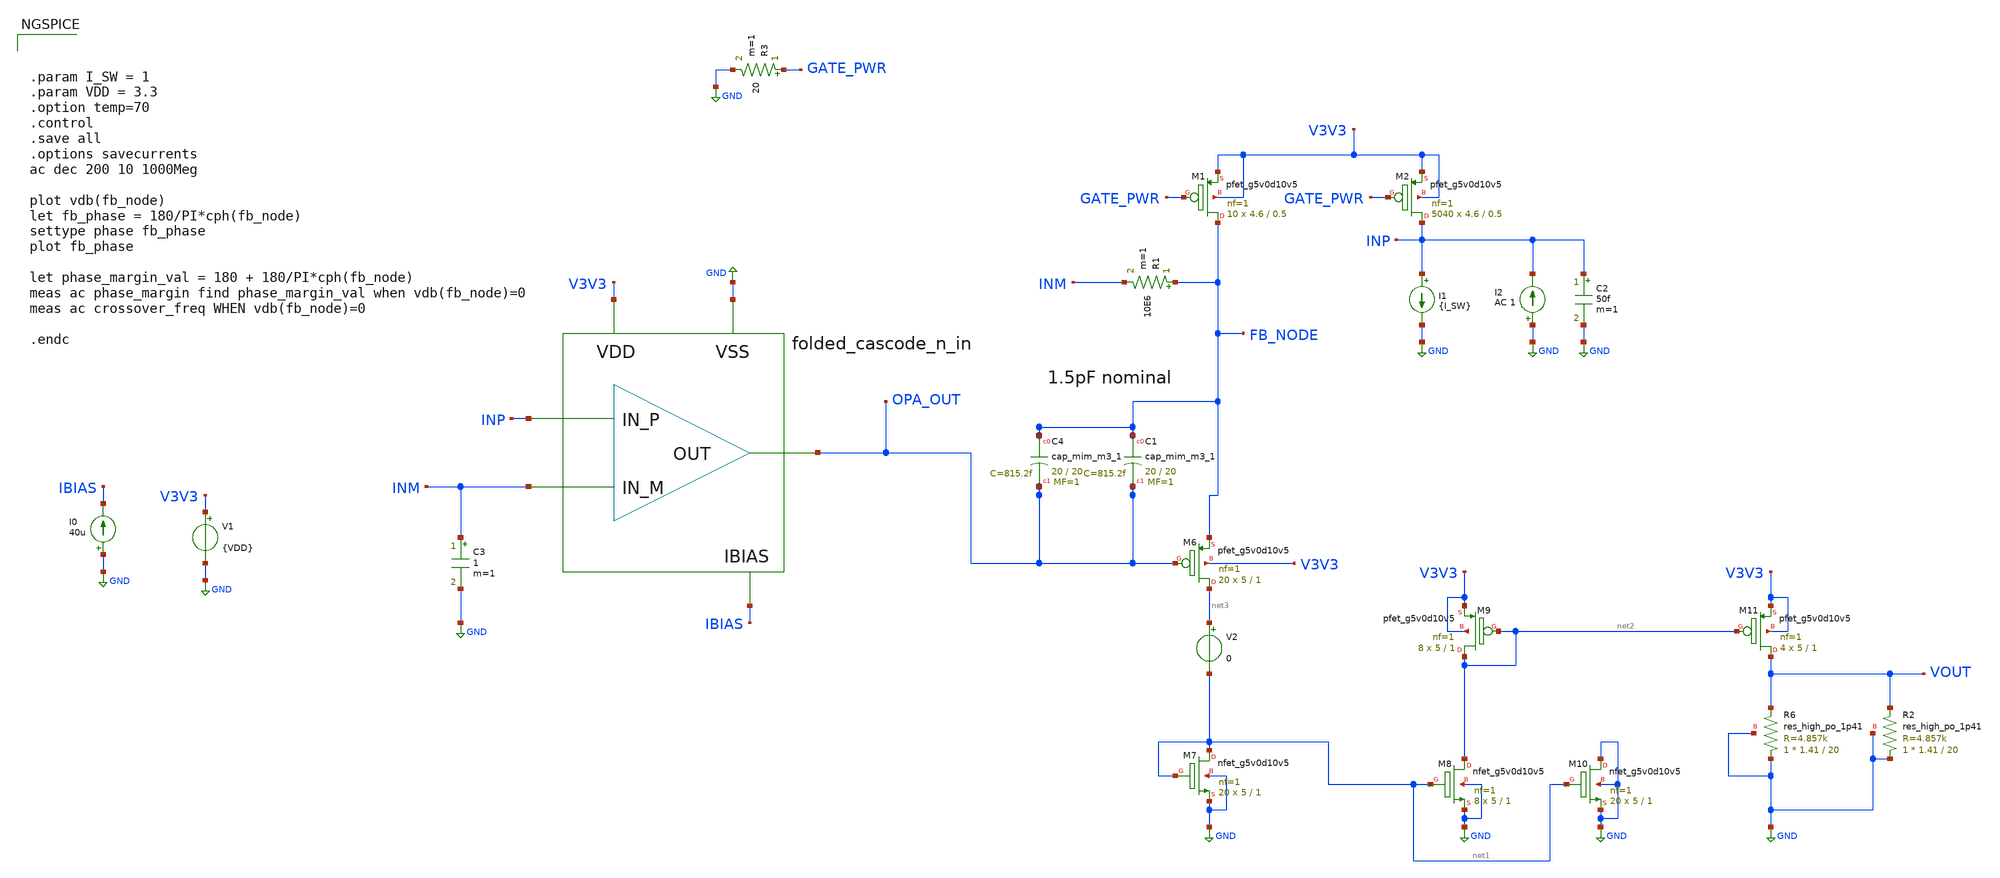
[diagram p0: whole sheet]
** sch_path: design/current-sense/current_sense_ac_phase_margin.sch
**.subckt current_sense_ac_phase_margin
V1 V3V3 GND {VDD}
I0 GND IBIAS 40u
x1 INP INM OPA_OUT V3V3 GND IBIAS folded_cascode_n_in
XM1 FB_NODE GATE_PWR V3V3 V3V3 sky130_fd_pr__pfet_g5v0d10v5 L=0.5 W=4.6 nf=1 ad='int((nf+1)/2) * W/nf * 0.29'
+ as='int((nf+2)/2) * W/nf * 0.29' pd='2*int((nf+1)/2) * (W/nf + 0.29)' ps='2*int((nf+2)/2) * (W/nf + 0.29)'
+ nrd='0.29 / W' nrs='0.29 / W' sa=0 sb=0 sd=0 mult=10 m=10
XM2 INP GATE_PWR V3V3 V3V3 sky130_fd_pr__pfet_g5v0d10v5 L=0.5 W=4.6 nf=1 ad='int((nf+1)/2) * W/nf * 0.29'
+ as='int((nf+2)/2) * W/nf * 0.29' pd='2*int((nf+1)/2) * (W/nf + 0.29)' ps='2*int((nf+2)/2) * (W/nf + 0.29)'
+ nrd='0.29 / W' nrs='0.29 / W' sa=0 sb=0 sd=0 mult=5040 m=5040
R3 GATE_PWR GND 20 m=1
I1 INP GND {I_SW}
I2 GND INP AC 1
C2 INP GND 50f m=1
XM6 net3 OPA_OUT FB_NODE V3V3 sky130_fd_pr__pfet_g5v0d10v5 L=1 W=5 nf=1 ad='int((nf+1)/2) * W/nf * 0.29'
+ as='int((nf+2)/2) * W/nf * 0.29' pd='2*int((nf+1)/2) * (W/nf + 0.29)' ps='2*int((nf+2)/2) * (W/nf + 0.29)'
+ nrd='0.29 / W' nrs='0.29 / W' sa=0 sb=0 sd=0 mult=20 m=20
XM7 net1 net1 GND GND sky130_fd_pr__nfet_g5v0d10v5 L=1 W=5 nf=1 ad='int((nf+1)/2) * W/nf * 0.29' as='int((nf+2)/2) * W/nf * 0.29'
+ pd='2*int((nf+1)/2) * (W/nf + 0.29)' ps='2*int((nf+2)/2) * (W/nf + 0.29)' nrd='0.29 / W' nrs='0.29 / W'
+ sa=0 sb=0 sd=0 mult=20 m=20
XM8 net2 net1 GND GND sky130_fd_pr__nfet_g5v0d10v5 L=1 W=5 nf=1 ad='int((nf+1)/2) * W/nf * 0.29' as='int((nf+2)/2) * W/nf * 0.29'
+ pd='2*int((nf+1)/2) * (W/nf + 0.29)' ps='2*int((nf+2)/2) * (W/nf + 0.29)' nrd='0.29 / W' nrs='0.29 / W'
+ sa=0 sb=0 sd=0 mult=8 m=8
XM9 net2 net2 V3V3 V3V3 sky130_fd_pr__pfet_g5v0d10v5 L=1 W=5 nf=1 ad='int((nf+1)/2) * W/nf * 0.29' as='int((nf+2)/2) * W/nf * 0.29'
+ pd='2*int((nf+1)/2) * (W/nf + 0.29)' ps='2*int((nf+2)/2) * (W/nf + 0.29)' nrd='0.29 / W' nrs='0.29 / W'
+ sa=0 sb=0 sd=0 mult=8 m=8
XM10 GND net1 GND GND sky130_fd_pr__nfet_g5v0d10v5 L=1 W=5 nf=1 ad='int((nf+1)/2) * W/nf * 0.29' as='int((nf+2)/2) * W/nf * 0.29'
+ pd='2*int((nf+1)/2) * (W/nf + 0.29)' ps='2*int((nf+2)/2) * (W/nf + 0.29)' nrd='0.29 / W' nrs='0.29 / W'
+ sa=0 sb=0 sd=0 mult=20 m=20
XM11 VOUT net2 V3V3 V3V3 sky130_fd_pr__pfet_g5v0d10v5 L=1 W=5 nf=1 ad='int((nf+1)/2) * W/nf * 0.29' as='int((nf+2)/2) * W/nf * 0.29'
+ pd='2*int((nf+1)/2) * (W/nf + 0.29)' ps='2*int((nf+2)/2) * (W/nf + 0.29)' nrd='0.29 / W' nrs='0.29 / W'
+ sa=0 sb=0 sd=0 mult=4 m=4
XR6 GND VOUT GND sky130_fd_pr__res_high_po_1p41 L=20 mult=1 m=1
XR2 GND VOUT GND sky130_fd_pr__res_high_po_1p41 L=20 mult=1 m=1
V2 net3 net1 0
XC4 FB_NODE OPA_OUT sky130_fd_pr__cap_mim_m3_1 W=20 L=20 MF=1 m=1
XC1 FB_NODE OPA_OUT sky130_fd_pr__cap_mim_m3_1 W=20 L=20 MF=1 m=1
R1 FB_NODE INM 10E6 m=1
C3 INM GND 1 m=1
**** begin user architecture code



.param I_SW = 1
.param VDD = 3.3
.option temp=70
.control
.save all
.options savecurrents
ac dec 200 10 1000Meg

plot vdb(fb_node)
let fb_phase = 180/PI*cph(fb_node)
settype phase fb_phase
plot fb_phase

let phase_margin_val = 180 + 180/PI*cph(fb_node)
meas ac phase_margin find phase_margin_val when vdb(fb_node)=0
meas ac crossover_freq WHEN vdb(fb_node)=0

.endc



.lib $::SKYWATER_MODELS/models/sky130.lib.spice tt
.option wnflag=1

**** end user architecture code
**.ends

* expanding   symbol:  design/folded-cascode-n-in/folded_cascode_n_in.sym # of pins=6
** sym_path: design/folded-cascode-n-in/folded_cascode_n_in.sym
** sch_path: design/folded-cascode-n-in/folded_cascode_n_in.sch
.subckt folded_cascode_n_in IN_P IN_M OUT VDD VSS VBN
*.ipin IN_P
*.ipin IN_M
*.ipin OUT
*.ipin VDD
*.ipin VSS
*.ipin VBN
XM1 net1 VBN VSS VSS sky130_fd_pr__nfet_g5v0d10v5 L=1 W=5 nf=1 ad='int((nf+1)/2) * W/nf * 0.29' as='int((nf+2)/2) * W/nf * 0.29'
+ pd='2*int((nf+1)/2) * (W/nf + 0.29)' ps='2*int((nf+2)/2) * (W/nf + 0.29)' nrd='0.29 / W' nrs='0.29 / W'
+ sa=0 sb=0 sd=0 mult=12 m=12
XM3 VS1_P IN_M net1 VSS sky130_fd_pr__nfet_g5v0d10v5 L=1 W=5 nf=1 ad='int((nf+1)/2) * W/nf * 0.29' as='int((nf+2)/2) * W/nf * 0.29'
+ pd='2*int((nf+1)/2) * (W/nf + 0.29)' ps='2*int((nf+2)/2) * (W/nf + 0.29)' nrd='0.29 / W' nrs='0.29 / W'
+ sa=0 sb=0 sd=0 mult=24 m=24
XM4 VS1_M IN_P net1 VSS sky130_fd_pr__nfet_g5v0d10v5 L=1 W=5 nf=1 ad='int((nf+1)/2) * W/nf * 0.29' as='int((nf+2)/2) * W/nf * 0.29'
+ pd='2*int((nf+1)/2) * (W/nf + 0.29)' ps='2*int((nf+2)/2) * (W/nf + 0.29)' nrd='0.29 / W' nrs='0.29 / W'
+ sa=0 sb=0 sd=0 mult=24 m=24
XM9 net2 VCN net4 VSS sky130_fd_pr__nfet_g5v0d10v5 L=1 W=5 nf=1 ad='int((nf+1)/2) * W/nf * 0.29' as='int((nf+2)/2) * W/nf * 0.29'
+ pd='2*int((nf+1)/2) * (W/nf + 0.29)' ps='2*int((nf+2)/2) * (W/nf + 0.29)' nrd='0.29 / W' nrs='0.29 / W'
+ sa=0 sb=0 sd=0 mult=3 m=3
XM10 net3 net2 VSS VSS sky130_fd_pr__nfet_g5v0d10v5 L=1 W=5 nf=1 ad='int((nf+1)/2) * W/nf * 0.29' as='int((nf+2)/2) * W/nf * 0.29'
+ pd='2*int((nf+1)/2) * (W/nf + 0.29)' ps='2*int((nf+2)/2) * (W/nf + 0.29)' nrd='0.29 / W' nrs='0.29 / W'
+ sa=0 sb=0 sd=0 mult=3 m=3
XM11 net4 net2 VSS VSS sky130_fd_pr__nfet_g5v0d10v5 L=1 W=5 nf=1 ad='int((nf+1)/2) * W/nf * 0.29' as='int((nf+2)/2) * W/nf * 0.29'
+ pd='2*int((nf+1)/2) * (W/nf + 0.29)' ps='2*int((nf+2)/2) * (W/nf + 0.29)' nrd='0.29 / W' nrs='0.29 / W'
+ sa=0 sb=0 sd=0 mult=3 m=3
XM12 OUT VCN net3 VSS sky130_fd_pr__nfet_g5v0d10v5 L=1 W=5 nf=1 ad='int((nf+1)/2) * W/nf * 0.29' as='int((nf+2)/2) * W/nf * 0.29'
+ pd='2*int((nf+1)/2) * (W/nf + 0.29)' ps='2*int((nf+2)/2) * (W/nf + 0.29)' nrd='0.29 / W' nrs='0.29 / W'
+ sa=0 sb=0 sd=0 mult=3 m=3
XM5 VS1_P VBP_INT VDD VDD sky130_fd_pr__pfet_g5v0d10v5 L=1 W=5 nf=1 ad='int((nf+1)/2) * W/nf * 0.29'
+ as='int((nf+2)/2) * W/nf * 0.29' pd='2*int((nf+1)/2) * (W/nf + 0.29)' ps='2*int((nf+2)/2) * (W/nf + 0.29)'
+ nrd='0.29 / W' nrs='0.29 / W' sa=0 sb=0 sd=0 mult=9 m=9
XM13 VS1_M VBP_INT VDD VDD sky130_fd_pr__pfet_g5v0d10v5 L=1 W=5 nf=1 ad='int((nf+1)/2) * W/nf * 0.29'
+ as='int((nf+2)/2) * W/nf * 0.29' pd='2*int((nf+1)/2) * (W/nf + 0.29)' ps='2*int((nf+2)/2) * (W/nf + 0.29)'
+ nrd='0.29 / W' nrs='0.29 / W' sa=0 sb=0 sd=0 mult=9 m=9
XM17 VBP_INT VBN VSS VSS sky130_fd_pr__nfet_g5v0d10v5 L=1 W=5 nf=1 ad='int((nf+1)/2) * W/nf * 0.29' as='int((nf+2)/2) * W/nf * 0.29'
+ pd='2*int((nf+1)/2) * (W/nf + 0.29)' ps='2*int((nf+2)/2) * (W/nf + 0.29)' nrd='0.29 / W' nrs='0.29 / W'
+ sa=0 sb=0 sd=0 mult=1 m=1
XM18 VBP_INT VBP_INT VDD VDD sky130_fd_pr__pfet_g5v0d10v5 L=1 W=5 nf=1 ad='int((nf+1)/2) * W/nf * 0.29'
+ as='int((nf+2)/2) * W/nf * 0.29' pd='2*int((nf+1)/2) * (W/nf + 0.29)' ps='2*int((nf+2)/2) * (W/nf + 0.29)'
+ nrd='0.29 / W' nrs='0.29 / W' sa=0 sb=0 sd=0 mult=1 m=1
XM14 net2 VCP VS1_M VDD sky130_fd_pr__pfet_g5v0d10v5 L=1 W=5 nf=1 ad='int((nf+1)/2) * W/nf * 0.29' as='int((nf+2)/2) * W/nf * 0.29'
+ pd='2*int((nf+1)/2) * (W/nf + 0.29)' ps='2*int((nf+2)/2) * (W/nf + 0.29)' nrd='0.29 / W' nrs='0.29 / W'
+ sa=0 sb=0 sd=0 mult=3 m=3
XM19 OUT VCP VS1_P VDD sky130_fd_pr__pfet_g5v0d10v5 L=1 W=5 nf=1 ad='int((nf+1)/2) * W/nf * 0.29' as='int((nf+2)/2) * W/nf * 0.29'
+ pd='2*int((nf+1)/2) * (W/nf + 0.29)' ps='2*int((nf+2)/2) * (W/nf + 0.29)' nrd='0.29 / W' nrs='0.29 / W'
+ sa=0 sb=0 sd=0 mult=3 m=3
XM2 VBP_INT VBP_INT VS1_P VSS sky130_fd_pr__nfet_g5v0d10v5 L=1 W=5 nf=1 ad='int((nf+1)/2) * W/nf * 0.29'
+ as='int((nf+2)/2) * W/nf * 0.29' pd='2*int((nf+1)/2) * (W/nf + 0.29)' ps='2*int((nf+2)/2) * (W/nf + 0.29)'
+ nrd='0.29 / W' nrs='0.29 / W' sa=0 sb=0 sd=0 mult=1 m=1
XM6 VBP_INT VBP_INT VS1_M VSS sky130_fd_pr__nfet_g5v0d10v5 L=1 W=5 nf=1 ad='int((nf+1)/2) * W/nf * 0.29'
+ as='int((nf+2)/2) * W/nf * 0.29' pd='2*int((nf+1)/2) * (W/nf + 0.29)' ps='2*int((nf+2)/2) * (W/nf + 0.29)'
+ nrd='0.29 / W' nrs='0.29 / W' sa=0 sb=0 sd=0 mult=1 m=1
XM7 VBP VBP VDD VDD sky130_fd_pr__pfet_g5v0d10v5 L=1 W=5 nf=1 ad='int((nf+1)/2) * W/nf * 0.29' as='int((nf+2)/2) * W/nf * 0.29'
+ pd='2*int((nf+1)/2) * (W/nf + 0.29)' ps='2*int((nf+2)/2) * (W/nf + 0.29)' nrd='0.29 / W' nrs='0.29 / W'
+ sa=0 sb=0 sd=0 mult=1 m=1
XM8 net5 VBP net12 VDD sky130_fd_pr__pfet_g5v0d10v5 L=1 W=5 nf=1 ad='int((nf+1)/2) * W/nf * 0.29' as='int((nf+2)/2) * W/nf * 0.29'
+ pd='2*int((nf+1)/2) * (W/nf + 0.29)' ps='2*int((nf+2)/2) * (W/nf + 0.29)' nrd='0.29 / W' nrs='0.29 / W'
+ sa=0 sb=0 sd=0 mult=1 m=1
XM15 VCN VBP VDD VDD sky130_fd_pr__pfet_g5v0d10v5 L=1 W=5 nf=1 ad='int((nf+1)/2) * W/nf * 0.29' as='int((nf+2)/2) * W/nf * 0.29'
+ pd='2*int((nf+1)/2) * (W/nf + 0.29)' ps='2*int((nf+2)/2) * (W/nf + 0.29)' nrd='0.29 / W' nrs='0.29 / W'
+ sa=0 sb=0 sd=0 mult=1 m=1
XM16 net5 net5 net6 VSS sky130_fd_pr__nfet_g5v0d10v5 L=1 W=5 nf=1 ad='int((nf+1)/2) * W/nf * 0.29' as='int((nf+2)/2) * W/nf * 0.29'
+ pd='2*int((nf+1)/2) * (W/nf + 0.29)' ps='2*int((nf+2)/2) * (W/nf + 0.29)' nrd='0.29 / W' nrs='0.29 / W'
+ sa=0 sb=0 sd=0 mult=2 m=2
XM20 net6 net5 VSS VSS sky130_fd_pr__nfet_g5v0d10v5 L=1 W=5 nf=1 ad='int((nf+1)/2) * W/nf * 0.29' as='int((nf+2)/2) * W/nf * 0.29'
+ pd='2*int((nf+1)/2) * (W/nf + 0.29)' ps='2*int((nf+2)/2) * (W/nf + 0.29)' nrd='0.29 / W' nrs='0.29 / W'
+ sa=0 sb=0 sd=0 mult=1 m=1
XM21 VCN VCN net6 VSS sky130_fd_pr__nfet_g5v0d10v5 L=1 W=5 nf=1 ad='int((nf+1)/2) * W/nf * 0.29' as='int((nf+2)/2) * W/nf * 0.29'
+ pd='2*int((nf+1)/2) * (W/nf + 0.29)' ps='2*int((nf+2)/2) * (W/nf + 0.29)' nrd='0.29 / W' nrs='0.29 / W'
+ sa=0 sb=0 sd=0 mult=1 m=1
XM24 net7 VBN net10 VSS sky130_fd_pr__nfet_g5v0d10v5 L=1 W=5 nf=1 ad='int((nf+1)/2) * W/nf * 0.29' as='int((nf+2)/2) * W/nf * 0.29'
+ pd='2*int((nf+1)/2) * (W/nf + 0.29)' ps='2*int((nf+2)/2) * (W/nf + 0.29)' nrd='0.29 / W' nrs='0.29 / W'
+ sa=0 sb=0 sd=0 mult=1 m=1
XM25 VCP VBN VSS VSS sky130_fd_pr__nfet_g5v0d10v5 L=1 W=5 nf=1 ad='int((nf+1)/2) * W/nf * 0.29' as='int((nf+2)/2) * W/nf * 0.29'
+ pd='2*int((nf+1)/2) * (W/nf + 0.29)' ps='2*int((nf+2)/2) * (W/nf + 0.29)' nrd='0.29 / W' nrs='0.29 / W'
+ sa=0 sb=0 sd=0 mult=1 m=1
XM26 net7 net7 net8 VDD sky130_fd_pr__pfet_g5v0d10v5 L=1 W=5 nf=1 ad='int((nf+1)/2) * W/nf * 0.29' as='int((nf+2)/2) * W/nf * 0.29'
+ pd='2*int((nf+1)/2) * (W/nf + 0.29)' ps='2*int((nf+2)/2) * (W/nf + 0.29)' nrd='0.29 / W' nrs='0.29 / W'
+ sa=0 sb=0 sd=0 mult=2 m=2
XM27 VCP VCP net8 VDD sky130_fd_pr__pfet_g5v0d10v5 L=1 W=5 nf=1 ad='int((nf+1)/2) * W/nf * 0.29' as='int((nf+2)/2) * W/nf * 0.29'
+ pd='2*int((nf+1)/2) * (W/nf + 0.29)' ps='2*int((nf+2)/2) * (W/nf + 0.29)' nrd='0.29 / W' nrs='0.29 / W'
+ sa=0 sb=0 sd=0 mult=1 m=1
XM28 net8 net7 VDD VDD sky130_fd_pr__pfet_g5v0d10v5 L=1 W=5 nf=1 ad='int((nf+1)/2) * W/nf * 0.29' as='int((nf+2)/2) * W/nf * 0.29'
+ pd='2*int((nf+1)/2) * (W/nf + 0.29)' ps='2*int((nf+2)/2) * (W/nf + 0.29)' nrd='0.29 / W' nrs='0.29 / W'
+ sa=0 sb=0 sd=0 mult=1 m=1
XM29 VBP VBN VSS VSS sky130_fd_pr__nfet_g5v0d10v5 L=1 W=5 nf=1 ad='int((nf+1)/2) * W/nf * 0.29' as='int((nf+2)/2) * W/nf * 0.29'
+ pd='2*int((nf+1)/2) * (W/nf + 0.29)' ps='2*int((nf+2)/2) * (W/nf + 0.29)' nrd='0.29 / W' nrs='0.29 / W'
+ sa=0 sb=0 sd=0 mult=1 m=1
XM32 net12 VBP net9 VDD sky130_fd_pr__pfet_g5v0d10v5 L=1 W=5 nf=1 ad='int((nf+1)/2) * W/nf * 0.29' as='int((nf+2)/2) * W/nf * 0.29'
+ pd='2*int((nf+1)/2) * (W/nf + 0.29)' ps='2*int((nf+2)/2) * (W/nf + 0.29)' nrd='0.29 / W' nrs='0.29 / W'
+ sa=0 sb=0 sd=0 mult=1 m=1
XM33 net9 VBP VDD VDD sky130_fd_pr__pfet_g5v0d10v5 L=1 W=5 nf=1 ad='int((nf+1)/2) * W/nf * 0.29' as='int((nf+2)/2) * W/nf * 0.29'
+ pd='2*int((nf+1)/2) * (W/nf + 0.29)' ps='2*int((nf+2)/2) * (W/nf + 0.29)' nrd='0.29 / W' nrs='0.29 / W'
+ sa=0 sb=0 sd=0 mult=1 m=1
XM34 net10 VBN net11 VSS sky130_fd_pr__nfet_g5v0d10v5 L=1 W=5 nf=1 ad='int((nf+1)/2) * W/nf * 0.29' as='int((nf+2)/2) * W/nf * 0.29'
+ pd='2*int((nf+1)/2) * (W/nf + 0.29)' ps='2*int((nf+2)/2) * (W/nf + 0.29)' nrd='0.29 / W' nrs='0.29 / W'
+ sa=0 sb=0 sd=0 mult=1 m=1
XM35 net11 VBN VSS VSS sky130_fd_pr__nfet_g5v0d10v5 L=1 W=5 nf=1 ad='int((nf+1)/2) * W/nf * 0.29' as='int((nf+2)/2) * W/nf * 0.29'
+ pd='2*int((nf+1)/2) * (W/nf + 0.29)' ps='2*int((nf+2)/2) * (W/nf + 0.29)' nrd='0.29 / W' nrs='0.29 / W'
+ sa=0 sb=0 sd=0 mult=1 m=1
XM30 VBN VBN VSS VSS sky130_fd_pr__nfet_g5v0d10v5 L=1 W=5 nf=1 ad='int((nf+1)/2) * W/nf * 0.29' as='int((nf+2)/2) * W/nf * 0.29'
+ pd='2*int((nf+1)/2) * (W/nf + 0.29)' ps='2*int((nf+2)/2) * (W/nf + 0.29)' nrd='0.29 / W' nrs='0.29 / W'
+ sa=0 sb=0 sd=0 mult=1 m=1
.ends

.GLOBAL GND
**** begin user architecture code
[sky130_models]
**** end user architecture code
.end
